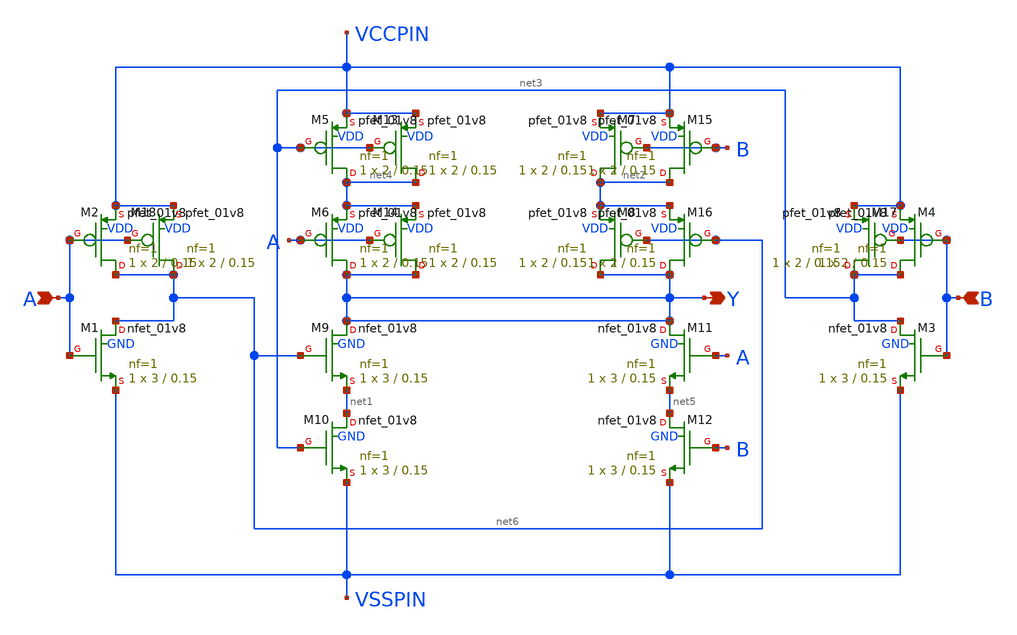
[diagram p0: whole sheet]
** sch_path: lib/xschem/XOR2X1.sch
**.subckt XOR2X1 A Y B
*.ipin A
*.opin Y
*.ipin B
XM1 net6 A VSSPIN GND sky130_fd_pr__nfet_01v8 L=0.15 W=3 nf=1 ad='int((nf+1)/2) * W/nf * 0.29' as='int((nf+2)/2) * W/nf * 0.29'
+ pd='2*int((nf+1)/2) * (W/nf + 0.29)' ps='2*int((nf+2)/2) * (W/nf + 0.29)' nrd='0.29 / W' nrs='0.29 / W'
+ sa=0 sb=0 sd=0 mult=1 m=1
XM2 net6 A VCCPIN VDD sky130_fd_pr__pfet_01v8 L=0.15 W=2 nf=1 ad='int((nf+1)/2) * W/nf * 0.29' as='int((nf+2)/2) * W/nf * 0.29'
+ pd='2*int((nf+1)/2) * (W/nf + 0.29)' ps='2*int((nf+2)/2) * (W/nf + 0.29)' nrd='0.29 / W' nrs='0.29 / W'
+ sa=0 sb=0 sd=0 mult=1 m=1
XM3 net3 B VSSPIN GND sky130_fd_pr__nfet_01v8 L=0.15 W=3 nf=1 ad='int((nf+1)/2) * W/nf * 0.29' as='int((nf+2)/2) * W/nf * 0.29'
+ pd='2*int((nf+1)/2) * (W/nf + 0.29)' ps='2*int((nf+2)/2) * (W/nf + 0.29)' nrd='0.29 / W' nrs='0.29 / W'
+ sa=0 sb=0 sd=0 mult=1 m=1
XM4 net3 B VCCPIN VDD sky130_fd_pr__pfet_01v8 L=0.15 W=2 nf=1 ad='int((nf+1)/2) * W/nf * 0.29' as='int((nf+2)/2) * W/nf * 0.29'
+ pd='2*int((nf+1)/2) * (W/nf + 0.29)' ps='2*int((nf+2)/2) * (W/nf + 0.29)' nrd='0.29 / W' nrs='0.29 / W'
+ sa=0 sb=0 sd=0 mult=1 m=1
XM5 net4 net3 VCCPIN VDD sky130_fd_pr__pfet_01v8 L=0.15 W=2 nf=1 ad='int((nf+1)/2) * W/nf * 0.29' as='int((nf+2)/2) * W/nf * 0.29'
+ pd='2*int((nf+1)/2) * (W/nf + 0.29)' ps='2*int((nf+2)/2) * (W/nf + 0.29)' nrd='0.29 / W' nrs='0.29 / W'
+ sa=0 sb=0 sd=0 mult=1 m=1
XM6 Y A net4 VDD sky130_fd_pr__pfet_01v8 L=0.15 W=2 nf=1 ad='int((nf+1)/2) * W/nf * 0.29' as='int((nf+2)/2) * W/nf * 0.29'
+ pd='2*int((nf+1)/2) * (W/nf + 0.29)' ps='2*int((nf+2)/2) * (W/nf + 0.29)' nrd='0.29 / W' nrs='0.29 / W'
+ sa=0 sb=0 sd=0 mult=1 m=1
XM7 net2 B VCCPIN VDD sky130_fd_pr__pfet_01v8 L=0.15 W=2 nf=1 ad='int((nf+1)/2) * W/nf * 0.29' as='int((nf+2)/2) * W/nf * 0.29'
+ pd='2*int((nf+1)/2) * (W/nf + 0.29)' ps='2*int((nf+2)/2) * (W/nf + 0.29)' nrd='0.29 / W' nrs='0.29 / W'
+ sa=0 sb=0 sd=0 mult=1 m=1
XM8 Y net6 net2 VDD sky130_fd_pr__pfet_01v8 L=0.15 W=2 nf=1 ad='int((nf+1)/2) * W/nf * 0.29' as='int((nf+2)/2) * W/nf * 0.29'
+ pd='2*int((nf+1)/2) * (W/nf + 0.29)' ps='2*int((nf+2)/2) * (W/nf + 0.29)' nrd='0.29 / W' nrs='0.29 / W'
+ sa=0 sb=0 sd=0 mult=1 m=1
XM9 Y net6 net1 GND sky130_fd_pr__nfet_01v8 L=0.15 W=3 nf=1 ad='int((nf+1)/2) * W/nf * 0.29' as='int((nf+2)/2) * W/nf * 0.29'
+ pd='2*int((nf+1)/2) * (W/nf + 0.29)' ps='2*int((nf+2)/2) * (W/nf + 0.29)' nrd='0.29 / W' nrs='0.29 / W'
+ sa=0 sb=0 sd=0 mult=1 m=1
XM10 net1 net3 VSSPIN GND sky130_fd_pr__nfet_01v8 L=0.15 W=3 nf=1 ad='int((nf+1)/2) * W/nf * 0.29' as='int((nf+2)/2) * W/nf * 0.29'
+ pd='2*int((nf+1)/2) * (W/nf + 0.29)' ps='2*int((nf+2)/2) * (W/nf + 0.29)' nrd='0.29 / W' nrs='0.29 / W'
+ sa=0 sb=0 sd=0 mult=1 m=1
XM11 Y A net5 GND sky130_fd_pr__nfet_01v8 L=0.15 W=3 nf=1 ad='int((nf+1)/2) * W/nf * 0.29' as='int((nf+2)/2) * W/nf * 0.29'
+ pd='2*int((nf+1)/2) * (W/nf + 0.29)' ps='2*int((nf+2)/2) * (W/nf + 0.29)' nrd='0.29 / W' nrs='0.29 / W'
+ sa=0 sb=0 sd=0 mult=1 m=1
XM12 net5 B VSSPIN GND sky130_fd_pr__nfet_01v8 L=0.15 W=3 nf=1 ad='int((nf+1)/2) * W/nf * 0.29' as='int((nf+2)/2) * W/nf * 0.29'
+ pd='2*int((nf+1)/2) * (W/nf + 0.29)' ps='2*int((nf+2)/2) * (W/nf + 0.29)' nrd='0.29 / W' nrs='0.29 / W'
+ sa=0 sb=0 sd=0 mult=1 m=1
XM13 net4 net3 VCCPIN VDD sky130_fd_pr__pfet_01v8 L=0.15 W=2 nf=1 ad='int((nf+1)/2) * W/nf * 0.29' as='int((nf+2)/2) * W/nf * 0.29'
+ pd='2*int((nf+1)/2) * (W/nf + 0.29)' ps='2*int((nf+2)/2) * (W/nf + 0.29)' nrd='0.29 / W' nrs='0.29 / W'
+ sa=0 sb=0 sd=0 mult=1 m=1
XM14 Y A net4 VDD sky130_fd_pr__pfet_01v8 L=0.15 W=2 nf=1 ad='int((nf+1)/2) * W/nf * 0.29' as='int((nf+2)/2) * W/nf * 0.29'
+ pd='2*int((nf+1)/2) * (W/nf + 0.29)' ps='2*int((nf+2)/2) * (W/nf + 0.29)' nrd='0.29 / W' nrs='0.29 / W'
+ sa=0 sb=0 sd=0 mult=1 m=1
XM15 net2 B VCCPIN VDD sky130_fd_pr__pfet_01v8 L=0.15 W=2 nf=1 ad='int((nf+1)/2) * W/nf * 0.29' as='int((nf+2)/2) * W/nf * 0.29'
+ pd='2*int((nf+1)/2) * (W/nf + 0.29)' ps='2*int((nf+2)/2) * (W/nf + 0.29)' nrd='0.29 / W' nrs='0.29 / W'
+ sa=0 sb=0 sd=0 mult=1 m=1
XM16 Y net6 net2 VDD sky130_fd_pr__pfet_01v8 L=0.15 W=2 nf=1 ad='int((nf+1)/2) * W/nf * 0.29' as='int((nf+2)/2) * W/nf * 0.29'
+ pd='2*int((nf+1)/2) * (W/nf + 0.29)' ps='2*int((nf+2)/2) * (W/nf + 0.29)' nrd='0.29 / W' nrs='0.29 / W'
+ sa=0 sb=0 sd=0 mult=1 m=1
XM17 net3 B VCCPIN VDD sky130_fd_pr__pfet_01v8 L=0.15 W=2 nf=1 ad='int((nf+1)/2) * W/nf * 0.29' as='int((nf+2)/2) * W/nf * 0.29'
+ pd='2*int((nf+1)/2) * (W/nf + 0.29)' ps='2*int((nf+2)/2) * (W/nf + 0.29)' nrd='0.29 / W' nrs='0.29 / W'
+ sa=0 sb=0 sd=0 mult=1 m=1
XM18 net6 A VCCPIN VDD sky130_fd_pr__pfet_01v8 L=0.15 W=2 nf=1 ad='int((nf+1)/2) * W/nf * 0.29' as='int((nf+2)/2) * W/nf * 0.29'
+ pd='2*int((nf+1)/2) * (W/nf + 0.29)' ps='2*int((nf+2)/2) * (W/nf + 0.29)' nrd='0.29 / W' nrs='0.29 / W'
+ sa=0 sb=0 sd=0 mult=1 m=1
**.ends
.end
